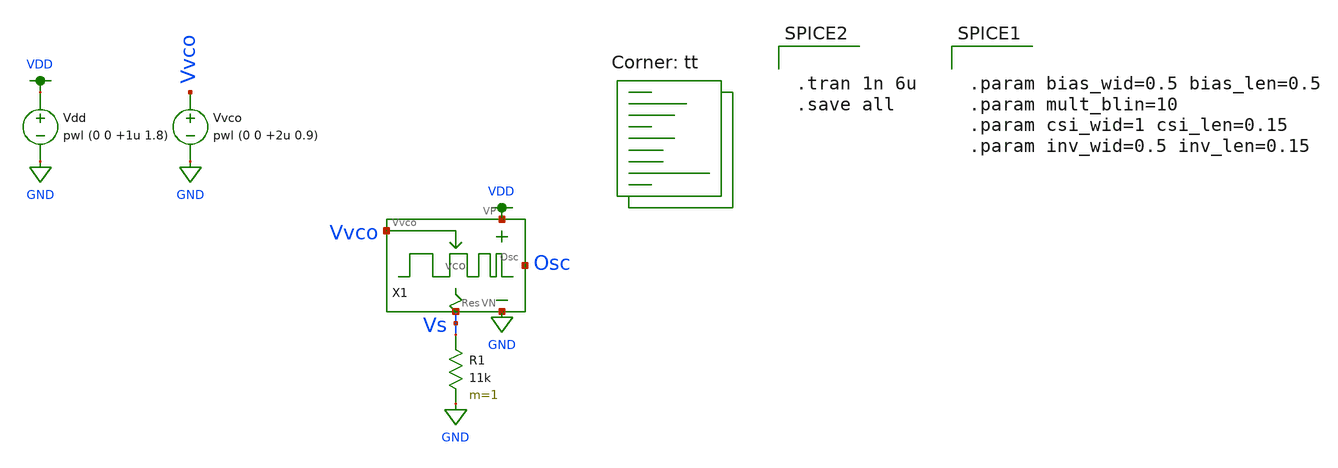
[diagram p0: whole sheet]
** sch_path: test_vco_final.sch
**.subckt test_vco_final
Vdd VDD GND pwl (0 0 +1u 1.8)
Vvco Vvco GND pwl (0 0 +2u 0.9)
R1 Vs GND 11k m=1
X1 VDD GND Vvco Osc Vs vco
**** begin user architecture code


.tran 1n 6u
.save all




.param bias_wid=0.5 bias_len=0.5
.param mult_blin=10
.param csi_wid=1 csi_len=0.15
.param inv_wid=0.5 inv_len=0.15


.lib $::SKYWATER_MODELS/sky130.lib.spice tt
**** end user architecture code
**.ends
.GLOBAL GND
.GLOBAL VDD
.end
